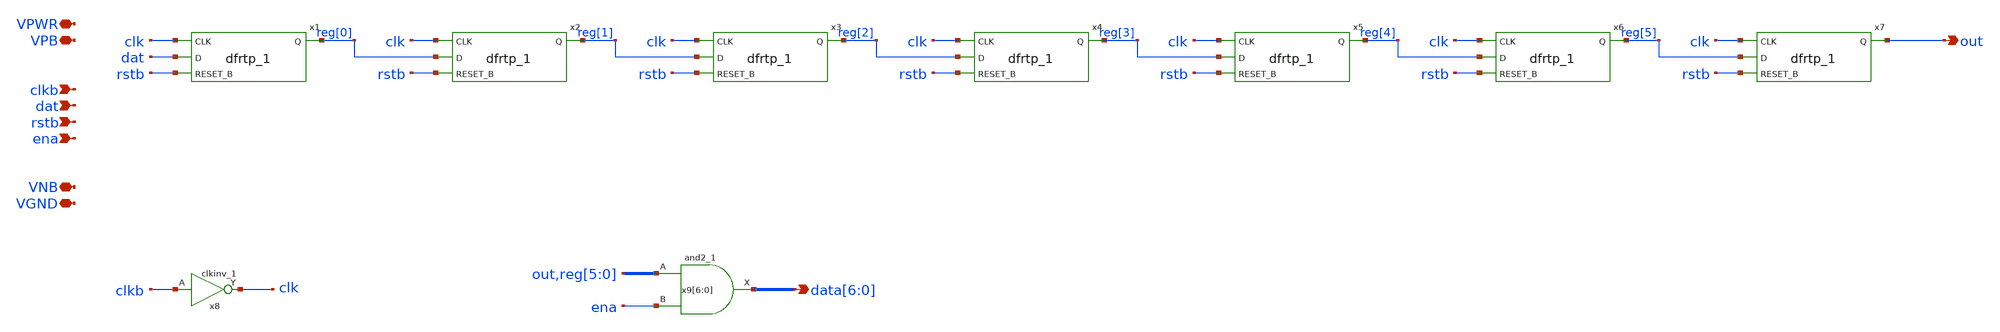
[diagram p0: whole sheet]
** sch_path: tt_um_mosbius/xschem/shift_reg_len7.sch
**.subckt shift_reg_len7 clkb dat rstb VPWR VGND
*+ data[6],data[5],data[4],data[3],data[2],data[1],data[0] ena out VPB VNB
*.ipin clkb
*.ipin dat
*.ipin rstb
*.iopin VPWR
*.iopin VGND
*.opin data[6],data[5],data[4],data[3],data[2],data[1],data[0]
*.ipin ena
*.opin out
*.iopin VPB
*.iopin VNB
x8 clkb VGND VNB VPB VPWR clk sky130_fd_sc_hd__clkinv_1
x9[6] out ena VGND VNB VPB VPWR data[6] sky130_fd_sc_hd__and2_1
x9[5] reg[5] ena VGND VNB VPB VPWR data[5] sky130_fd_sc_hd__and2_1
x9[4] reg[4] ena VGND VNB VPB VPWR data[4] sky130_fd_sc_hd__and2_1
x9[3] reg[3] ena VGND VNB VPB VPWR data[3] sky130_fd_sc_hd__and2_1
x9[2] reg[2] ena VGND VNB VPB VPWR data[2] sky130_fd_sc_hd__and2_1
x9[1] reg[1] ena VGND VNB VPB VPWR data[1] sky130_fd_sc_hd__and2_1
x9[0] reg[0] ena VGND VNB VPB VPWR data[0] sky130_fd_sc_hd__and2_1
x1 clk dat rstb VGND VNB VPB VPWR reg[0] sky130_fd_sc_hd__dfrtp_1
x2 clk reg[0] rstb VGND VNB VPB VPWR reg[1] sky130_fd_sc_hd__dfrtp_1
x3 clk reg[1] rstb VGND VNB VPB VPWR reg[2] sky130_fd_sc_hd__dfrtp_1
x4 clk reg[2] rstb VGND VNB VPB VPWR reg[3] sky130_fd_sc_hd__dfrtp_1
x5 clk reg[3] rstb VGND VNB VPB VPWR reg[4] sky130_fd_sc_hd__dfrtp_1
x6 clk reg[4] rstb VGND VNB VPB VPWR reg[5] sky130_fd_sc_hd__dfrtp_1
x7 clk reg[5] rstb VGND VNB VPB VPWR out sky130_fd_sc_hd__dfrtp_1
**.ends
.end
